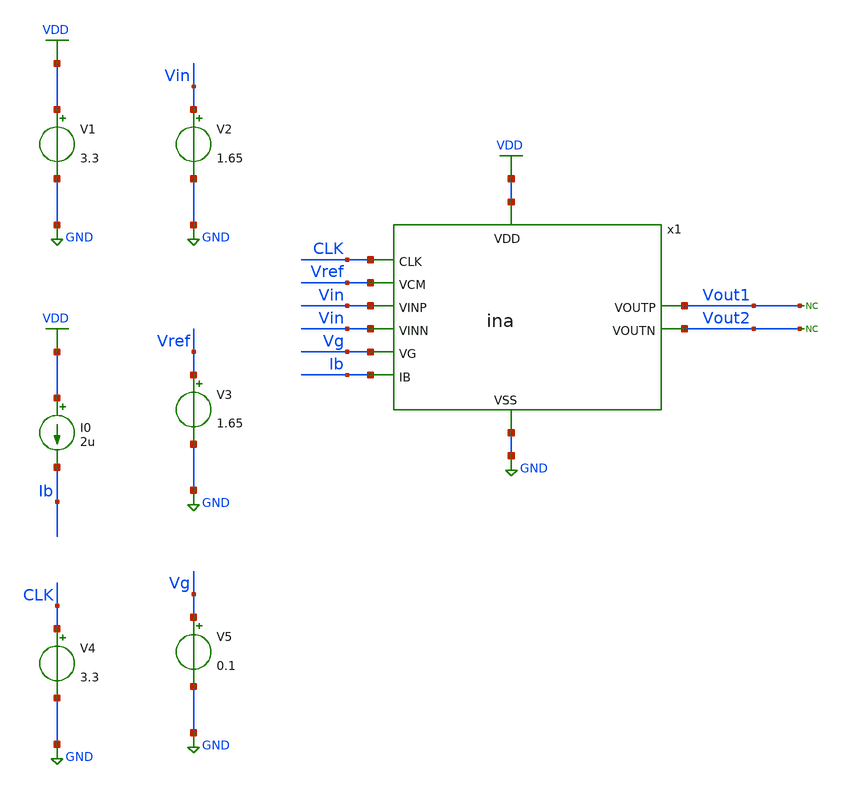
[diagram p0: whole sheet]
** sch_path: designs/libs/tb_ina/tb_ina_dc/tb_ina_dc.sch
**.subckt tb_ina_dc
V1 VDD GND 3.3
V2 Vin GND 1.65
I0 VDD Ib 2u
V3 Vref GND 1.65
V4 CLK GND 3.3
V5 Vg GND 0.1
* noconn Vout1
* noconn Vout2
x1 Vg VDD Vin Vin CLK Vout1 Vout2 GND Vref Ib ina
**** begin user architecture code

.include $::180MCU_MODELS/design.ngspice
.lib $::180MCU_MODELS/sm141064.ngspice typical
.lib $::180MCU_MODELS/sm141064.ngspice cap_mim
.lib $::180MCU_MODELS/sm141064.ngspice moscap_typical
.lib $::180MCU_MODELS/sm141064.ngspice mimcap_typical
.lib $::180MCU_MODELS/sm141064.ngspice res_typical
* .lib $::180MCU_MODELS/sm141064.ngspice res_statistical
* ngspice commands




.control
save all

run
set color0 = white

*************************************
** PARAMETERS
*************************************

let Vdd  = 3.3
let Vcm  = Vdd/2
let Ibias = 2u
let Vg = 0.1

*************************************
** SOURCES
*************************************

alter @V1[DC] = $&Vdd
alter @V2[DC] = 0
alter @V3[DC] = $&Vcm
alter @I0[DC] = $&Ibias
alter @V4[DC] = $&Vdd
alter @V5[DC] = $&Vg

*************************************
** DC SWEEP SIMULATION
*************************************

dc V2 0 3.3 0.1

*************************************
** PLOTS
*************************************

setplot dc1
let vout1 = v(Vout1)
let vout2 = v(Vout2)
let vin = v(Vin)
let vout_diff = vout1-vout2
let vcm_out = (vout1+vout2)/2
plot vout_diff
plot vcm_out

*************************************
** SAVE
*************************************

write tb_ina_dc.raw

*************************************
** DC SWEEP SIMULATION2
*************************************

alter @V1[DC] = 0
alter @V2[DC] = $&Vcm
dc V1 0 3.5 0.1

setplot dc2
let vout1 = v(Vout1)
let vout2 = v(Vout2)
let vin = v(Vin)
let vcm_out = (vout1+vout2)/2
plot vcm_out

.endc
* ngspice commands



**** end user architecture code
**.ends
.GLOBAL GND
.GLOBAL VDD
.end
